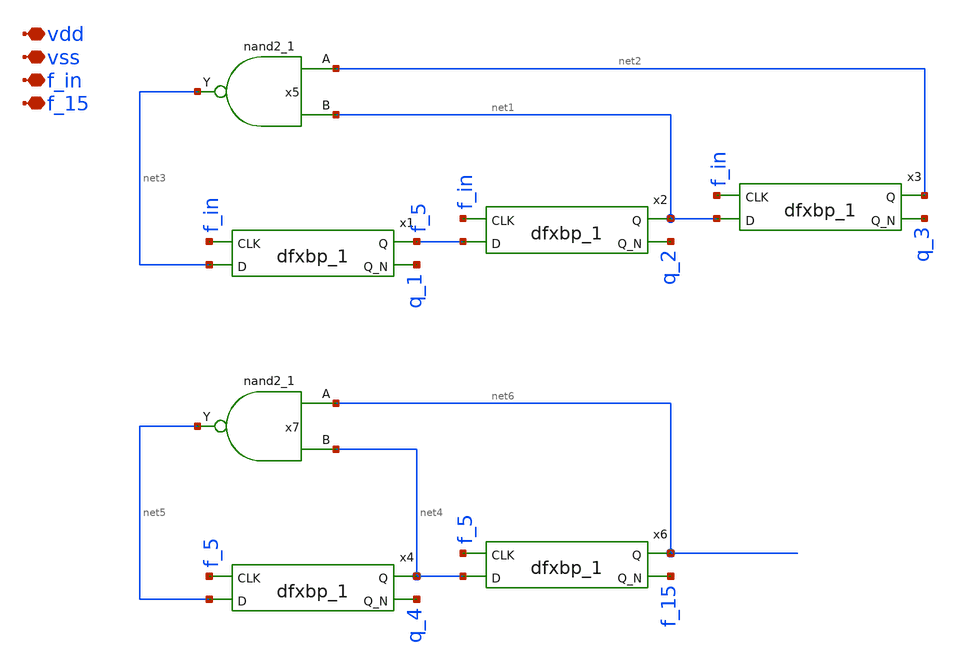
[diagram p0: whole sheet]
** sch_path: xschem/d_ff_15.sch
**.subckt d_ff_15 vdd vss f_in f_15
*.iopin vdd
*.iopin vss
*.iopin f_in
*.iopin f_15
x1 f_in net3 vss vss vdd vdd f_5 q_1 sky130_fd_sc_hd__dfxbp_1
x5 net2 net1 vss vss vdd vdd net3 sky130_fd_sc_hd__nand2_1
x2 f_in f_5 vss vss vdd vdd net1 q_2 sky130_fd_sc_hd__dfxbp_1
x3 f_in net1 vss vss vdd vdd net2 q_3 sky130_fd_sc_hd__dfxbp_1
x4 f_5 net5 vss vss vdd vdd net4 q_4 sky130_fd_sc_hd__dfxbp_1
x6 f_5 net4 vss vss vdd vdd net6 f_15 sky130_fd_sc_hd__dfxbp_1
x7 net6 net4 vss vss vdd vdd net5 sky130_fd_sc_hd__nand2_1
**.ends
.end
